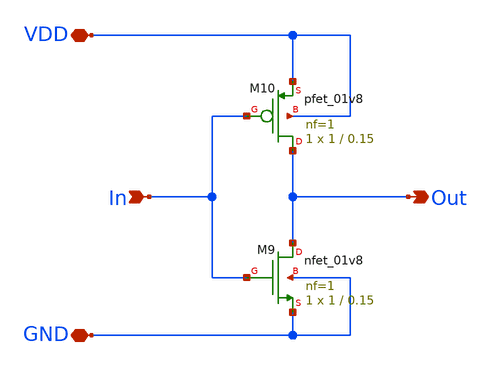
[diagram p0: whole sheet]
** sch_path: schematics/Layouting/inverter_symbol.sch
**.subckt inverter_symbol In Out VDD GND
*.ipin In
*.opin Out
*.iopin VDD
*.iopin GND
XM9 Out In GND GND sky130_fd_pr__nfet_01v8 L=0.15 W=1 nf=1 ad='int((nf+1)/2) * W/nf * 0.29' as='int((nf+2)/2) * W/nf * 0.29'
+ pd='2*int((nf+1)/2) * (W/nf + 0.29)' ps='2*int((nf+2)/2) * (W/nf + 0.29)' nrd='0.29 / W' nrs='0.29 / W'
+ sa=0 sb=0 sd=0 mult=1 m=1
XM10 Out In VDD VDD sky130_fd_pr__pfet_01v8 L=0.15 W=1 nf=1 ad='int((nf+1)/2) * W/nf * 0.29' as='int((nf+2)/2) * W/nf * 0.29'
+ pd='2*int((nf+1)/2) * (W/nf + 0.29)' ps='2*int((nf+2)/2) * (W/nf + 0.29)' nrd='0.29 / W' nrs='0.29 / W'
+ sa=0 sb=0 sd=0 mult=1 m=1
**.ends
.end
